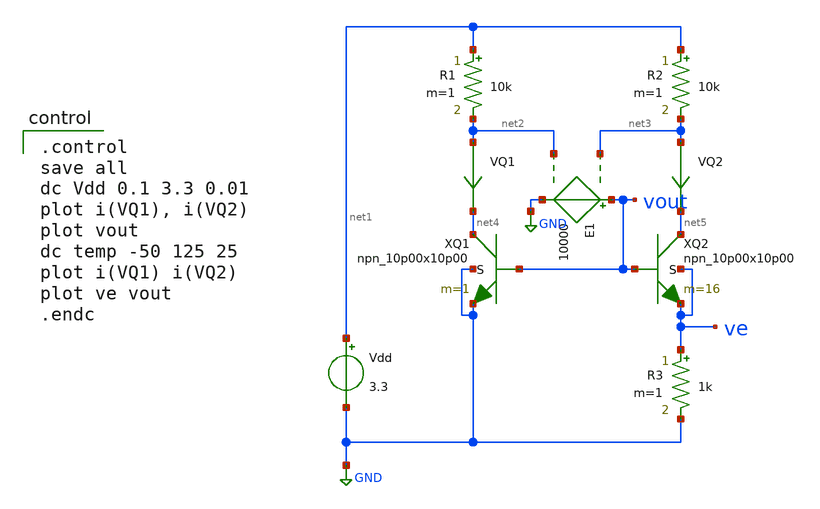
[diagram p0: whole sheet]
** sch_path: bgr/bjt-ptat.sch
**.subckt bjt-ptat
XQ1 net4 vout GND GND npn_10p00x10p00 m=1
Vdd net1 GND 3.3
XQ2 net5 vout ve ve npn_10p00x10p00 m=16
R3 ve GND 1k m=1
R1 net1 net2 10k m=1
R2 net1 net3 10k m=1
E1 vout GND net3 net2 10000
VQ1 net2 net4 0
.save i(vq1)
VQ2 net3 net5 0
.save i(vq2)
**** begin user architecture code

.include $::180MCU_MODELS/design.ngspice
.lib $::180MCU_MODELS/sm141064.ngspice typical
.lib $::180MCU_MODELS/sm141064.ngspice res_typical
.lib $::180MCU_MODELS/sm141064.ngspice moscap_typical
.lib $::180MCU_MODELS/sm141064.ngspice bjt_typical
* .lib $::180MCU_MODELS/sm141064.ngspice res_statistical


.control
save all
dc Vdd 0.1 3.3 0.01
plot i(VQ1), i(VQ2)
plot vout
dc temp -50 125 25
plot i(VQ1) i(VQ2)
plot ve vout
.endc

**** end user architecture code
**.ends
.GLOBAL GND
.end
